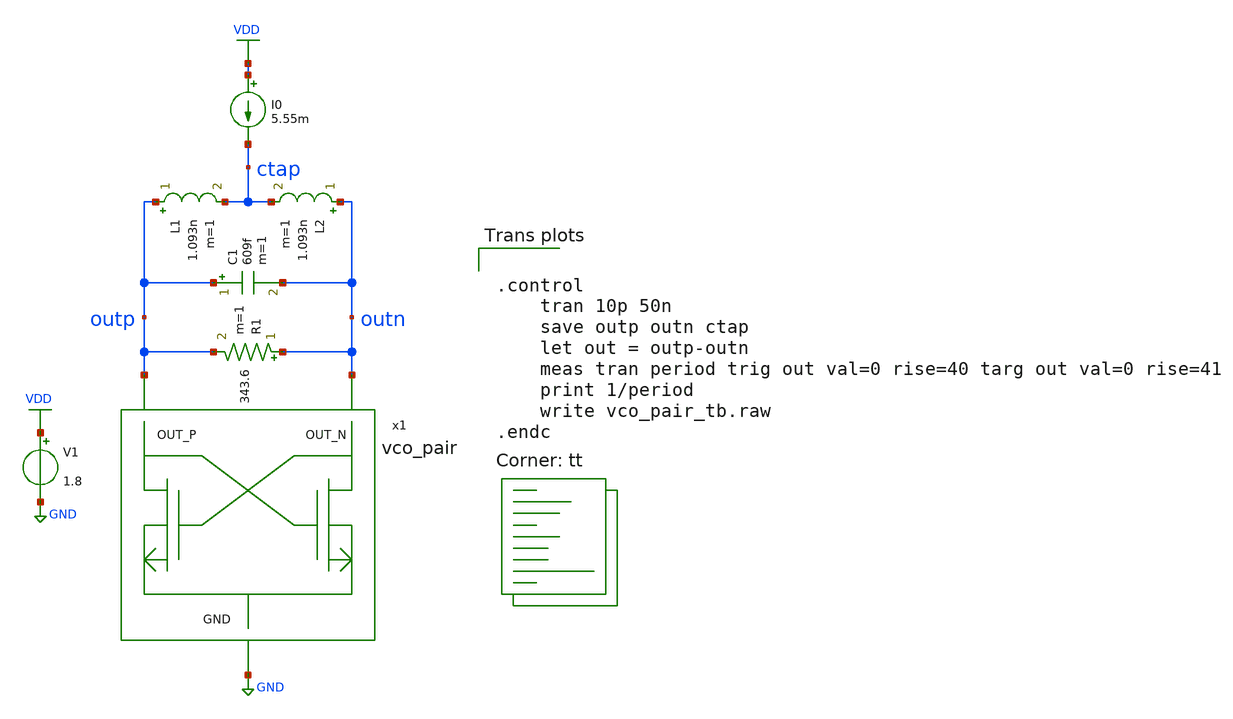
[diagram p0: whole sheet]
** sch_path: xschem/vco/testbenches/vco_pair/vco_pair_tb.sch
* YI/C9Shc8z/CWPKLJb8BQD+O4ziO4wpAwbu7u7s7HEAy2IIt2IIlQD6O4ziO4ypAAICtDl/GPL8AgNZy7Go7vwAAAAAAAAAAAAAAAAAAAAAAAPeMn2NHvywNosQhFFq
**.subckt vco_pair_tb
x1 outp outn GND vco_pair
R1 outn outp 343.6 m=1
C1 outp outn 609f m=1
L1 outp ctap 1.093n m=1
L2 outn ctap 1.093n m=1
I0 VDD ctap 5.55m
V1 VDD GND 1.8
**** begin user architecture code


.control
    tran 10p 50n
    save outp outn ctap
    let out = outp-outn
    meas tran period trig out val=0 rise=40 targ out val=0 rise=41
    print 1/period
    write vco_pair_tb.raw
.endc


.lib $::SKYWATER_MODELS/sky130.lib.spice tt
**** end user architecture code
**.ends
.GLOBAL VDD
.GLOBAL GND
.end
